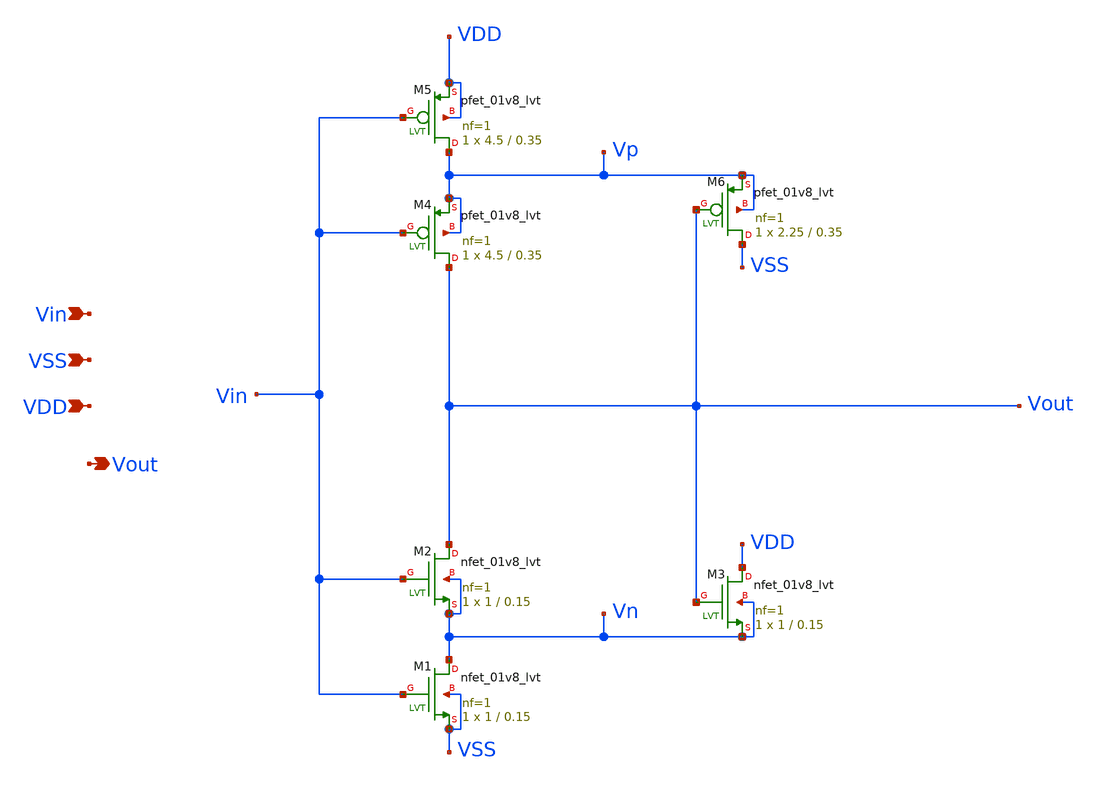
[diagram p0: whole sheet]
** sch_path: xschem/T1/schmitt_trigger/schm_trig.sch
**.subckt schm_trig Vin VDD VSS Vout
*.ipin Vin
*.ipin VDD
*.ipin VSS
*.opin Vout
XM5 Vp Vin VDD VDD sky130_fd_pr__pfet_01v8_lvt L=0.35 W=4.5 nf=1 ad='int((1 + 1)/2) * 4.5 / 1 * 0.29'
+ as='int((1 + 2)/2) * 4.5 / 1 * 0.29' pd='2*int((1 + 1)/2) * (4.5 / 1 + 0.29)' ps='2*int((1 + 2)/2) * (4.5 / 1 + 0.29)'
+ nrd='0.29 / 4.5 ' nrs='0.29 / 4.5 ' sa=0 sb=0 sd=0 mult=1 m=1
XM4 Vout Vin Vp Vp sky130_fd_pr__pfet_01v8_lvt L=0.35 W=4.5 nf=1 ad='int((1 + 1)/2) * 4.5 / 1 * 0.29'
+ as='int((1 + 2)/2) * 4.5 / 1 * 0.29' pd='2*int((1 + 1)/2) * (4.5 / 1 + 0.29)' ps='2*int((1 + 2)/2) * (4.5 / 1 + 0.29)'
+ nrd='0.29 / 4.5 ' nrs='0.29 / 4.5 ' sa=0 sb=0 sd=0 mult=1 m=1
XM6 VSS Vout Vp Vp sky130_fd_pr__pfet_01v8_lvt L=0.35 W=2.25 nf=1 ad='int((1 + 1)/2) * 2.25 / 1 * 0.29'
+ as='int((1 + 2)/2) * 2.25 / 1 * 0.29' pd='2*int((1 + 1)/2) * (2.25 / 1 + 0.29)' ps='2*int((1 + 2)/2) * (2.25 / 1 + 0.29)'
+ nrd='0.29 / 2.25 ' nrs='0.29 / 2.25 ' sa=0 sb=0 sd=0 mult=1 m=1
XM2 Vout Vin Vn Vn sky130_fd_pr__nfet_01v8_lvt L=0.15 W=1 nf=1 ad='int((1 + 1)/2) * 1 / 1 * 0.29' as='int((1 + 2)/2) * 1 / 1 * 0.29'
+ pd='2*int((1 + 1)/2) * (1 / 1 + 0.29)' ps='2*int((1 + 2)/2) * (1 / 1 + 0.29)' nrd='0.29 / 1 ' nrs='0.29 / 1 '
+ sa=0 sb=0 sd=0 mult=1 m=1
XM1 Vn Vin VSS VSS sky130_fd_pr__nfet_01v8_lvt L=0.15 W=1 nf=1 ad='int((1 + 1)/2) * 1 / 1 * 0.29' as='int((1 + 2)/2) * 1 / 1 * 0.29'
+ pd='2*int((1 + 1)/2) * (1 / 1 + 0.29)' ps='2*int((1 + 2)/2) * (1 / 1 + 0.29)' nrd='0.29 / 1 ' nrs='0.29 / 1 '
+ sa=0 sb=0 sd=0 mult=1 m=1
XM3 VDD Vout Vn Vn sky130_fd_pr__nfet_01v8_lvt L=0.15 W=1 nf=1 ad='int((1 + 1)/2) * 1 / 1 * 0.29' as='int((1 + 2)/2) * 1 / 1 * 0.29'
+ pd='2*int((1 + 1)/2) * (1 / 1 + 0.29)' ps='2*int((1 + 2)/2) * (1 / 1 + 0.29)' nrd='0.29 / 1 ' nrs='0.29 / 1 '
+ sa=0 sb=0 sd=0 mult=1 m=1
**.ends
.end
